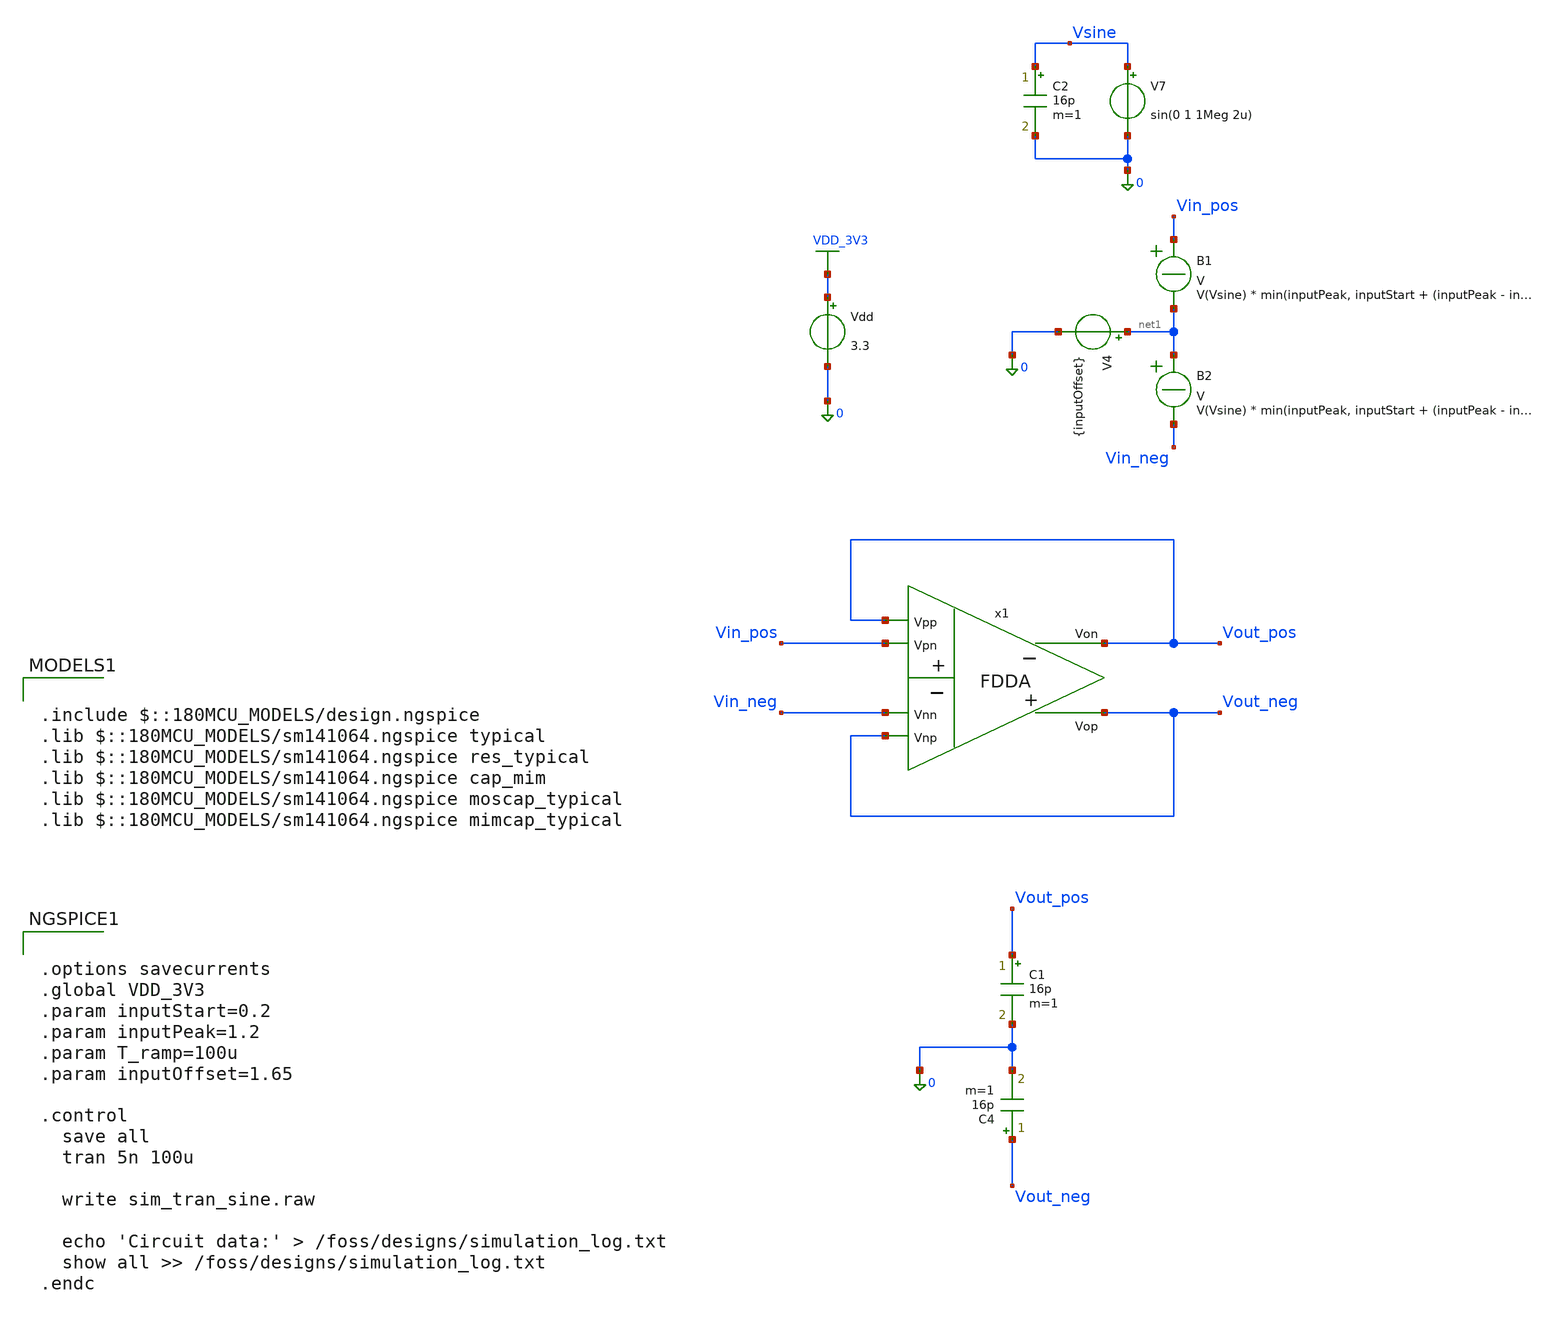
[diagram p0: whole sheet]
** sch_path: src/sim/sim_tran_sine.sch
**.subckt sim_tran_sine
Vdd VDD_3V3 0 3.3
.save i(vdd)
C1 Vout_pos 0 16p m=1
C4 Vout_neg 0 16p m=1
x1 Vout_pos Vout_neg Vout_neg Vin_neg Vout_pos Vin_pos fdda_subckt
V4 net1 0 {inputOffset}
.save i(v4)
V7 Vsine 0 sin(0 1 1Meg 2u)
.save i(v7)
C2 Vsine 0 16p m=1
B1 Vin_pos net1 V = V(Vsine) * min(inputPeak, inputStart + (inputPeak - inputStart) * (time/T_ramp))
B2 net1 Vin_neg V = V(Vsine) * min(inputPeak, inputStart + (inputPeak - inputStart) * (time/T_ramp))
**** begin user architecture code

.include $::180MCU_MODELS/design.ngspice
.lib $::180MCU_MODELS/sm141064.ngspice typical
.lib $::180MCU_MODELS/sm141064.ngspice res_typical
.lib $::180MCU_MODELS/sm141064.ngspice cap_mim
.lib $::180MCU_MODELS/sm141064.ngspice moscap_typical
.lib $::180MCU_MODELS/sm141064.ngspice mimcap_typical




.options savecurrents
.global VDD_3V3
.param inputStart=0.2
.param inputPeak=1.2
.param T_ramp=100u
.param inputOffset=1.65

.control
  save all
  tran 5n 100u

  write sim_tran_sine.raw

  echo 'Circuit data:' > /foss/designs/simulation_log.txt
  show all >> /foss/designs/simulation_log.txt
.endc


**** end user architecture code
**.ends
.GLOBAL VDD_3V3
.end
